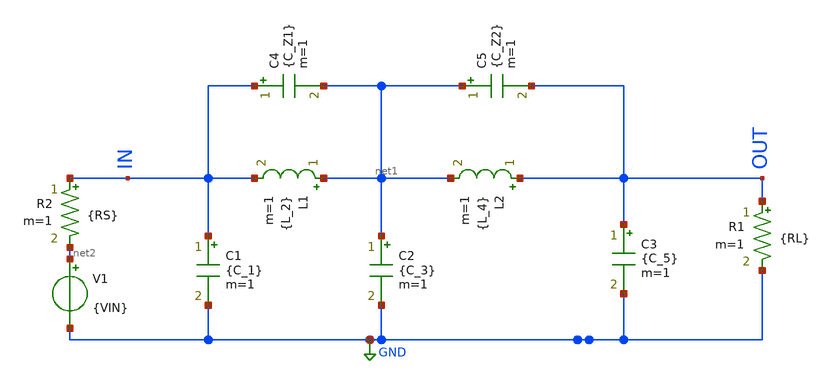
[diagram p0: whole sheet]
** sch_path: LPF design/SCLICAP_TEST/LC_ladder.sch
**.subckt LC_ladder
L1 net1 IN {L_2} m=1
L2 OUT net1 {L_4} m=1
C1 IN GND {C_1} m=1
C2 net1 GND {C_3} m=1
R1 OUT GND {RL} m=1
R2 IN net2 {RS} m=1
V1 net2 GND {VIN}
C3 OUT GND {C_5} m=1
C4 IN net1 {C_Z1} m=1
C5 net1 OUT {C_Z2} m=1
**.ends
.GLOBAL GND
.end
